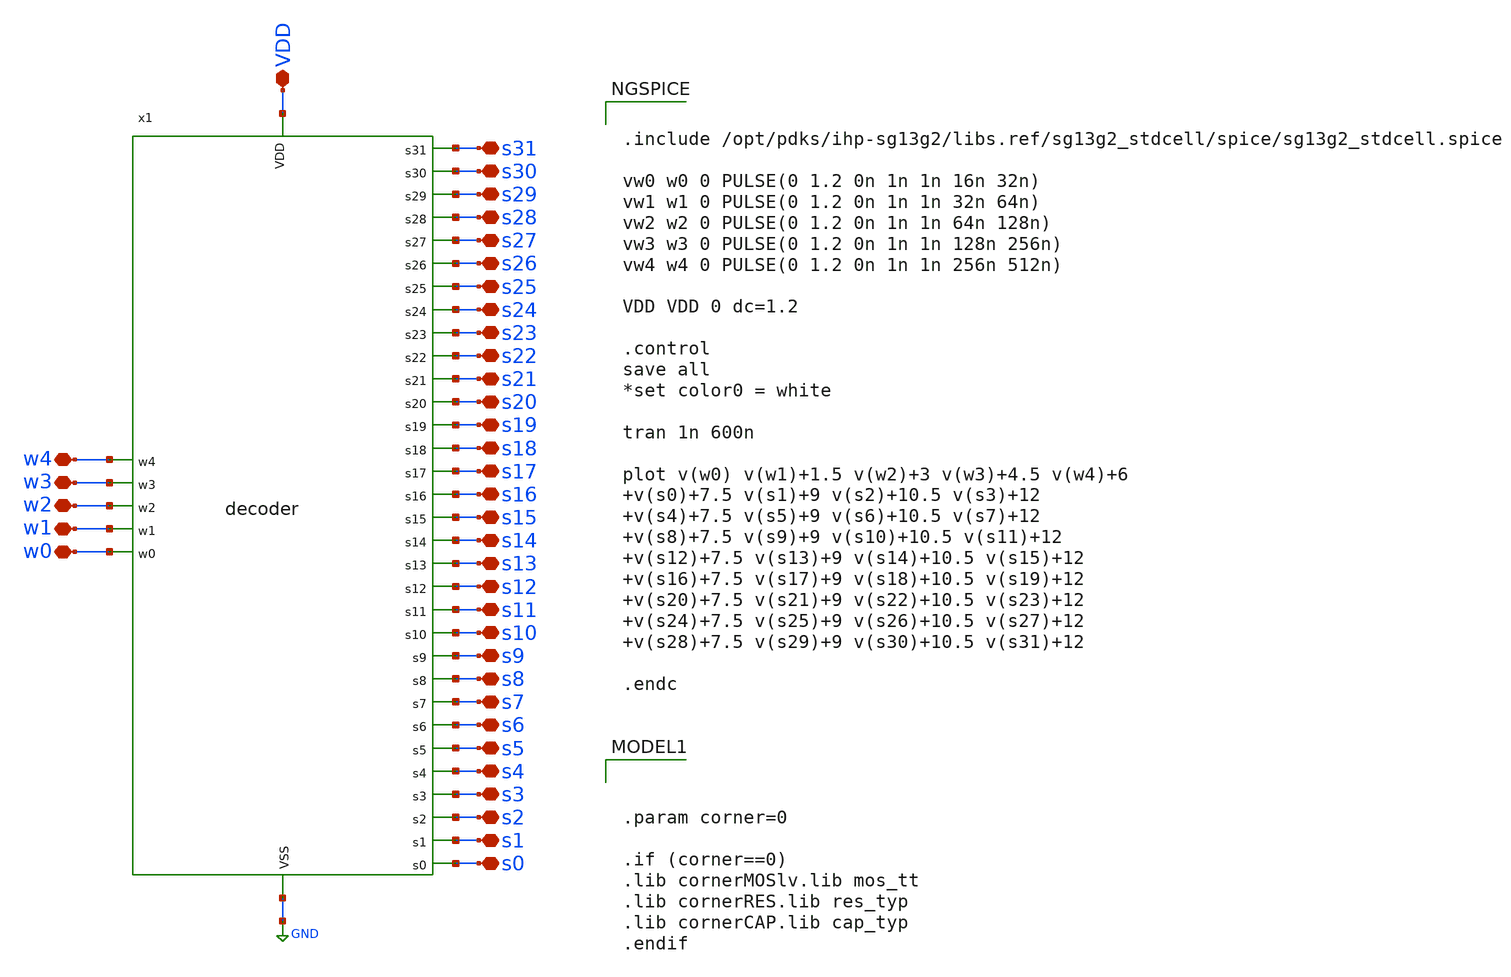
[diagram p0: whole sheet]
** sch_path: src/digital/tb_decoder.sch
**.subckt tb_decoder s0 s1 s2 s3 s4 s5 s6 s7 s8 s9 s10 s11 s12 s13 s14 s15 s16 s17 s18 s19 s20 s21
*+ s22 s23 s24 s25 s26 s27 s28 s29 s30 s31 w4 w3 w2 w1 w0 VDD
*.iopin s0
*.iopin s1
*.iopin s2
*.iopin s3
*.iopin s4
*.iopin s5
*.iopin s6
*.iopin s7
*.iopin s8
*.iopin s9
*.iopin s10
*.iopin s11
*.iopin s12
*.iopin s13
*.iopin s14
*.iopin s15
*.iopin s16
*.iopin s17
*.iopin s18
*.iopin s19
*.iopin s20
*.iopin s21
*.iopin s22
*.iopin s23
*.iopin s24
*.iopin s25
*.iopin s26
*.iopin s27
*.iopin s28
*.iopin s29
*.iopin s30
*.iopin s31
*.iopin w4
*.iopin w3
*.iopin w2
*.iopin w1
*.iopin w0
*.iopin VDD
x1 w2 w3 w0 w1 w4 s31 s30 s29 s28 s27 s26 s25 s24 s23 s22 s21 s20 s19 s18 s17 s16 s15 s14 s13 s12
+ s11 s10 s9 s8 s7 s6 s5 s4 s3 s2 s1 s0 VDD GND decoder
**** begin user architecture code


.include /opt/pdks/ihp-sg13g2/libs.ref/sg13g2_stdcell/spice/sg13g2_stdcell.spice

vw0 w0 0 PULSE(0 1.2 0n 1n 1n 16n 32n)
vw1 w1 0 PULSE(0 1.2 0n 1n 1n 32n 64n)
vw2 w2 0 PULSE(0 1.2 0n 1n 1n 64n 128n)
vw3 w3 0 PULSE(0 1.2 0n 1n 1n 128n 256n)
vw4 w4 0 PULSE(0 1.2 0n 1n 1n 256n 512n)

VDD VDD 0 dc=1.2

.control
save all
*set color0 = white

tran 1n 600n

plot v(w0) v(w1)+1.5 v(w2)+3 v(w3)+4.5 v(w4)+6 v(s0)+7.5 v(s1)+9 v(s2)+10.5 v(s3)+12 v(s4)+7.5
+ v(s5)+9 v(s6)+10.5 v(s7)+12 v(s8)+7.5 v(s9)+9 v(s10)+10.5 v(s11)+12 v(s12)+7.5 v(s13)+9 v(s14)+10.5
+ v(s15)+12 v(s16)+7.5 v(s17)+9 v(s18)+10.5 v(s19)+12 v(s20)+7.5 v(s21)+9 v(s22)+10.5 v(s23)+12 v(s24)+7.5
+ v(s25)+9 v(s26)+10.5 v(s27)+12 v(s28)+7.5 v(s29)+9 v(s30)+10.5 v(s31)+12

.endc




.param corner=0

.if (corner==0)
.lib cornerMOSlv.lib mos_tt
.lib cornerRES.lib res_typ
.lib cornerCAP.lib cap_typ
.endif

**** end user architecture code
**.ends

* expanding   symbol:
*+  /home/designer/shared/ihp-sg13g2_ana_mux_32_1_serial_sel/src/digital/decoder.sym # of pins=39
** sym_path: xschem/digital/decoder.sym
** sch_path: xschem/digital/decoder.sch
.subckt decoder w2 w3 w0 w1 w4 s31 s30 s29 s28 s27 s26 s25 s24 s23 s22 s21 s20 s19 s18 s17 s16 s15
+ s14 s13 s12 s11 s10 s9 s8 s7 s6 s5 s4 s3 s2 s1 s0 VDD VSS
*.opin s3
*.opin s0
*.opin s1
*.opin s2
*.opin s4
*.opin s5
*.opin s9
*.opin s6
*.opin s7
*.opin s8
*.opin s10
*.opin s11
*.opin s15
*.opin s12
*.opin s13
*.opin s14
*.opin s16
*.opin s17
*.opin s21
*.opin s18
*.opin s19
*.opin s20
*.opin s22
*.opin s23
*.opin s24
*.opin s25
*.opin s29
*.opin s26
*.opin s27
*.opin s28
*.opin s30
*.opin s31
*.ipin w4
*.ipin w3
*.ipin w2
*.ipin w1
*.ipin w0
*.ipin VDD
*.ipin VSS
x1 net1 w0 VDD VSS sg13g2_inv_1
x2 net2 w1 VDD VSS sg13g2_inv_1
x3 net5 w2 VDD VSS sg13g2_inv_1
x4 net3 w3 VDD VSS sg13g2_inv_1
x5 net4 w4 VDD VSS sg13g2_inv_1
x7 net6 net1 net2 net5 net3 VDD VSS sg13g2_and4_1
x8 s0 net6 net4 VDD VSS sg13g2_and2_1
x9 net7 w0 net2 net5 net3 VDD VSS sg13g2_and4_1
x10 s1 net7 net4 VDD VSS sg13g2_and2_1
x11 net8 net1 w1 net5 net3 VDD VSS sg13g2_and4_1
x12 s2 net8 net4 VDD VSS sg13g2_and2_1
x13 net9 w0 w1 net5 net3 VDD VSS sg13g2_and4_1
x14 s3 net9 net4 VDD VSS sg13g2_and2_1
x15 net10 net1 net2 w2 net3 VDD VSS sg13g2_and4_1
x16 s4 net10 net4 VDD VSS sg13g2_and2_1
x17 net11 w0 net2 w2 net3 VDD VSS sg13g2_and4_1
x18 s5 net11 net4 VDD VSS sg13g2_and2_1
x19 net12 net1 w1 w2 net3 VDD VSS sg13g2_and4_1
x20 s6 net12 net4 VDD VSS sg13g2_and2_1
x21 net13 w0 w1 w2 net3 VDD VSS sg13g2_and4_1
x22 s7 net13 net4 VDD VSS sg13g2_and2_1
x23 net14 net1 net2 net5 w3 VDD VSS sg13g2_and4_1
x24 s8 net14 net4 VDD VSS sg13g2_and2_1
x25 net15 w0 net2 net5 w3 VDD VSS sg13g2_and4_1
x26 s9 net15 net4 VDD VSS sg13g2_and2_1
x27 net16 net1 w1 net5 w3 VDD VSS sg13g2_and4_1
x28 s10 net16 net4 VDD VSS sg13g2_and2_1
x29 net17 w0 w1 net5 w3 VDD VSS sg13g2_and4_1
x30 s11 net17 net4 VDD VSS sg13g2_and2_1
x31 net18 net1 net2 w2 w3 VDD VSS sg13g2_and4_1
x32 s12 net18 net4 VDD VSS sg13g2_and2_1
x33 net19 w0 net2 w2 w3 VDD VSS sg13g2_and4_1
x34 s13 net19 net4 VDD VSS sg13g2_and2_1
x35 net20 net1 w1 w2 w3 VDD VSS sg13g2_and4_1
x36 s14 net20 net4 VDD VSS sg13g2_and2_1
x37 net21 w0 w1 w2 w3 VDD VSS sg13g2_and4_1
x38 s15 net21 net4 VDD VSS sg13g2_and2_1
x39 net22 net1 net2 net5 net3 VDD VSS sg13g2_and4_1
x40 s16 net22 w4 VDD VSS sg13g2_and2_1
x41 net23 w0 net2 net5 net3 VDD VSS sg13g2_and4_1
x42 s17 net23 w4 VDD VSS sg13g2_and2_1
x43 net24 net1 w1 net5 net3 VDD VSS sg13g2_and4_1
x44 s18 net24 w4 VDD VSS sg13g2_and2_1
x45 net25 w0 w1 net5 net3 VDD VSS sg13g2_and4_1
x46 s19 net25 w4 VDD VSS sg13g2_and2_1
x47 net26 net1 net2 w2 net3 VDD VSS sg13g2_and4_1
x48 s20 net26 w4 VDD VSS sg13g2_and2_1
x49 net27 w0 net2 w2 net3 VDD VSS sg13g2_and4_1
x50 s21 net27 w4 VDD VSS sg13g2_and2_1
x51 net28 net1 w1 w2 net3 VDD VSS sg13g2_and4_1
x52 s22 net28 w4 VDD VSS sg13g2_and2_1
x53 net29 w0 w1 w2 net3 VDD VSS sg13g2_and4_1
x54 s23 net29 w4 VDD VSS sg13g2_and2_1
x55 net30 net1 net2 net5 w3 VDD VSS sg13g2_and4_1
x56 s24 net30 w4 VDD VSS sg13g2_and2_1
x57 net31 w0 net2 net5 w3 VDD VSS sg13g2_and4_1
x58 s25 net31 w4 VDD VSS sg13g2_and2_1
x59 net32 net1 w1 net5 w3 VDD VSS sg13g2_and4_1
x60 s26 net32 w4 VDD VSS sg13g2_and2_1
x61 net33 w0 w1 net5 w3 VDD VSS sg13g2_and4_1
x62 s27 net33 w4 VDD VSS sg13g2_and2_1
x63 net34 net1 net2 w2 w3 VDD VSS sg13g2_and4_1
x64 s28 net34 w4 VDD VSS sg13g2_and2_1
x65 net35 w0 net2 w2 w3 VDD VSS sg13g2_and4_1
x66 s29 net35 w4 VDD VSS sg13g2_and2_1
x67 net36 net1 w1 w2 w3 VDD VSS sg13g2_and4_1
x68 s30 net36 w4 VDD VSS sg13g2_and2_1
x69 net37 w0 w1 w2 w3 VDD VSS sg13g2_and4_1
x70 s31 net37 w4 VDD VSS sg13g2_and2_1
.ends


* expanding   symbol:  sg13g2_stdcells/sg13g2_inv_1.sym # of pins=2
** sym_path: sg13g2_stdcells/sg13g2_inv_1.sym
** sch_path: sg13g2_stdcells/sg13g2_inv_1.sch
.subckt sg13g2_inv_1 Y A VDD VSS
*.opin Y
*.ipin A
*.iopin VDD
*.iopin VSS
XM1 Y A VSS VSS sg13_lv_nmos w=740.00n l=130.00n ng=1 m=1 mm_ok=1
XM2 Y A VDD VDD sg13_lv_pmos w=1.12u l=130.00n ng=1 m=1 mm_ok=1
.ends


* expanding   symbol:  sg13g2_stdcells/sg13g2_and4_1.sym # of pins=5
** sym_path: sg13g2_stdcells/sg13g2_and4_1.sym
** sch_path: sg13g2_stdcells/sg13g2_and4_1.sch
.subckt sg13g2_and4_1 X A B C D VDD VSS
*.ipin A
*.ipin B
*.ipin C
*.ipin D
*.opin X
*.iopin VDD
*.iopin VSS
XM1 net1 A net3 VSS sg13_lv_nmos w=640.00n l=130.00n ng=1 m=1 mm_ok=1
XM2 net3 B net2 VSS sg13_lv_nmos w=640.00n l=130.00n ng=1 m=1 mm_ok=1
XM3 net2 C net4 VSS sg13_lv_nmos w=640.00n l=130.00n ng=1 m=1 mm_ok=1
XM4 net4 D VSS VSS sg13_lv_nmos w=640.00n l=130.00n ng=1 m=1 mm_ok=1
XM5 X net1 VSS VSS sg13_lv_nmos w=740.00n l=130.00n ng=1 m=1 mm_ok=1
XM6 net1 D VDD VDD sg13_lv_pmos w=840.00n l=130.00n ng=1 m=1 mm_ok=1
XM7 net1 C VDD VDD sg13_lv_pmos w=840.00n l=130.00n ng=1 m=1 mm_ok=1
XM8 net1 B VDD VDD sg13_lv_pmos w=840.00n l=130.00n ng=1 m=1 mm_ok=1
XM9 net1 A VDD VDD sg13_lv_pmos w=840.00n l=130.00n ng=1 m=1 mm_ok=1
XM10 X net1 VDD VDD sg13_lv_pmos w=1.12u l=130.00n ng=1 m=1 mm_ok=1
.ends


* expanding   symbol:  sg13g2_stdcells/sg13g2_and2_1.sym # of pins=3
** sym_path: sg13g2_stdcells/sg13g2_and2_1.sym
** sch_path: sg13g2_stdcells/sg13g2_and2_1.sch
.subckt sg13g2_and2_1 X A B VDD VSS
*.ipin A
*.ipin B
*.opin X
*.iopin VDD
*.iopin VSS
XM1 net1 A net2 VSS sg13_lv_nmos w=640.00n l=130.00n ng=1 m=1 mm_ok=1
XM2 net2 B VSS VSS sg13_lv_nmos w=640.00n l=130.00n ng=1 m=1 mm_ok=1
XM3 X net1 VSS VSS sg13_lv_nmos w=740.00n l=130.00n ng=1 m=1 mm_ok=1
XM4 net1 B VDD VDD sg13_lv_pmos w=840.00n l=130.00n ng=1 m=1 mm_ok=1
XM5 net1 A VDD VDD sg13_lv_pmos w=840.00n l=130.00n ng=1 m=1 mm_ok=1
XM6 X net1 VDD VDD sg13_lv_pmos w=1.12u l=130.00n ng=1 m=1 mm_ok=1
.ends

.GLOBAL GND
.end
